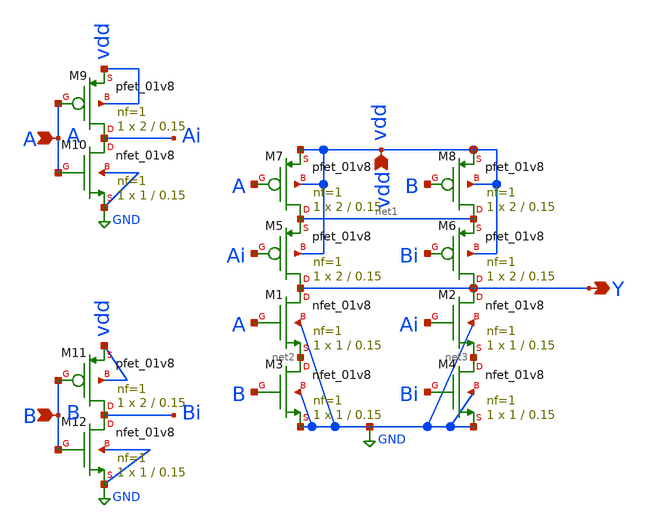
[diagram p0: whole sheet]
** sch_path: Circuit Files/Logic gate design using MOSFETS/gates/XOR_gate.sch
**.subckt XOR_gate Y A B vdd
*.opin Y
*.ipin A
*.ipin B
*.ipin vdd
XM1 Y A net2 GND sky130_fd_pr__nfet_01v8 L=0.15 W=1 nf=1 ad='int((nf+1)/2) * W/nf * 0.29' as='int((nf+2)/2) * W/nf * 0.29'
+ pd='2*int((nf+1)/2) * (W/nf + 0.29)' ps='2*int((nf+2)/2) * (W/nf + 0.29)' nrd='0.29 / W' nrs='0.29 / W'
+ sa=0 sb=0 sd=0 mult=1 m=1
XM2 Y Ai net3 GND sky130_fd_pr__nfet_01v8 L=0.15 W=1 nf=1 ad='int((nf+1)/2) * W/nf * 0.29' as='int((nf+2)/2) * W/nf * 0.29'
+ pd='2*int((nf+1)/2) * (W/nf + 0.29)' ps='2*int((nf+2)/2) * (W/nf + 0.29)' nrd='0.29 / W' nrs='0.29 / W'
+ sa=0 sb=0 sd=0 mult=1 m=1
XM3 net2 B GND GND sky130_fd_pr__nfet_01v8 L=0.15 W=1 nf=1 ad='int((nf+1)/2) * W/nf * 0.29' as='int((nf+2)/2) * W/nf * 0.29'
+ pd='2*int((nf+1)/2) * (W/nf + 0.29)' ps='2*int((nf+2)/2) * (W/nf + 0.29)' nrd='0.29 / W' nrs='0.29 / W'
+ sa=0 sb=0 sd=0 mult=1 m=1
XM4 net3 Bi GND GND sky130_fd_pr__nfet_01v8 L=0.15 W=1 nf=1 ad='int((nf+1)/2) * W/nf * 0.29' as='int((nf+2)/2) * W/nf * 0.29'
+ pd='2*int((nf+1)/2) * (W/nf + 0.29)' ps='2*int((nf+2)/2) * (W/nf + 0.29)' nrd='0.29 / W' nrs='0.29 / W'
+ sa=0 sb=0 sd=0 mult=1 m=1
XM5 Y Ai net1 vdd sky130_fd_pr__pfet_01v8 L=0.15 W=2 nf=1 ad='int((nf+1)/2) * W/nf * 0.29' as='int((nf+2)/2) * W/nf * 0.29'
+ pd='2*int((nf+1)/2) * (W/nf + 0.29)' ps='2*int((nf+2)/2) * (W/nf + 0.29)' nrd='0.29 / W' nrs='0.29 / W'
+ sa=0 sb=0 sd=0 mult=1 m=1
XM6 Y Bi net1 vdd sky130_fd_pr__pfet_01v8 L=0.15 W=2 nf=1 ad='int((nf+1)/2) * W/nf * 0.29' as='int((nf+2)/2) * W/nf * 0.29'
+ pd='2*int((nf+1)/2) * (W/nf + 0.29)' ps='2*int((nf+2)/2) * (W/nf + 0.29)' nrd='0.29 / W' nrs='0.29 / W'
+ sa=0 sb=0 sd=0 mult=1 m=1
XM7 net1 A vdd vdd sky130_fd_pr__pfet_01v8 L=0.15 W=2 nf=1 ad='int((nf+1)/2) * W/nf * 0.29' as='int((nf+2)/2) * W/nf * 0.29'
+ pd='2*int((nf+1)/2) * (W/nf + 0.29)' ps='2*int((nf+2)/2) * (W/nf + 0.29)' nrd='0.29 / W' nrs='0.29 / W'
+ sa=0 sb=0 sd=0 mult=1 m=1
XM8 net1 B vdd vdd sky130_fd_pr__pfet_01v8 L=0.15 W=2 nf=1 ad='int((nf+1)/2) * W/nf * 0.29' as='int((nf+2)/2) * W/nf * 0.29'
+ pd='2*int((nf+1)/2) * (W/nf + 0.29)' ps='2*int((nf+2)/2) * (W/nf + 0.29)' nrd='0.29 / W' nrs='0.29 / W'
+ sa=0 sb=0 sd=0 mult=1 m=1
XM9 Ai A vdd vdd sky130_fd_pr__pfet_01v8 L=0.15 W=2 nf=1 ad='int((nf+1)/2) * W/nf * 0.29' as='int((nf+2)/2) * W/nf * 0.29'
+ pd='2*int((nf+1)/2) * (W/nf + 0.29)' ps='2*int((nf+2)/2) * (W/nf + 0.29)' nrd='0.29 / W' nrs='0.29 / W'
+ sa=0 sb=0 sd=0 mult=1 m=1
XM10 Ai A GND GND sky130_fd_pr__nfet_01v8 L=0.15 W=1 nf=1 ad='int((nf+1)/2) * W/nf * 0.29' as='int((nf+2)/2) * W/nf * 0.29'
+ pd='2*int((nf+1)/2) * (W/nf + 0.29)' ps='2*int((nf+2)/2) * (W/nf + 0.29)' nrd='0.29 / W' nrs='0.29 / W'
+ sa=0 sb=0 sd=0 mult=1 m=1
XM11 Bi B vdd vdd sky130_fd_pr__pfet_01v8 L=0.15 W=2 nf=1 ad='int((nf+1)/2) * W/nf * 0.29' as='int((nf+2)/2) * W/nf * 0.29'
+ pd='2*int((nf+1)/2) * (W/nf + 0.29)' ps='2*int((nf+2)/2) * (W/nf + 0.29)' nrd='0.29 / W' nrs='0.29 / W'
+ sa=0 sb=0 sd=0 mult=1 m=1
XM12 Bi B GND GND sky130_fd_pr__nfet_01v8 L=0.15 W=1 nf=1 ad='int((nf+1)/2) * W/nf * 0.29' as='int((nf+2)/2) * W/nf * 0.29'
+ pd='2*int((nf+1)/2) * (W/nf + 0.29)' ps='2*int((nf+2)/2) * (W/nf + 0.29)' nrd='0.29 / W' nrs='0.29 / W'
+ sa=0 sb=0 sd=0 mult=1 m=1
**.ends
.GLOBAL GND
.end
